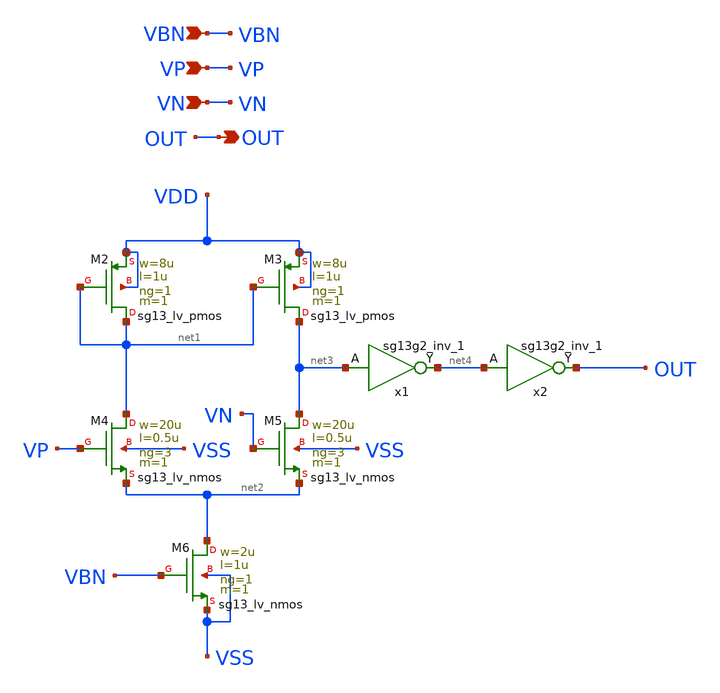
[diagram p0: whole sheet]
** sch_path: design/blocks/comparator/schematic/comp_sup.sch
**.subckt comp_sup OUT VN VP VBN
*.opin OUT
*.ipin VN
*.ipin VP
*.ipin VBN
XM2 net1 net1 VDD VDD sg13_lv_pmos w=8u l=1u ng=1 m=1 mm_ok=1
XM3 net3 net1 VDD VDD sg13_lv_pmos w=8u l=1u ng=1 m=1 mm_ok=1
XM4 net1 VP net2 VSS sg13_lv_nmos w=20u l=0.5u ng=3 m=1 mm_ok=1
XM5 net3 VN net2 VSS sg13_lv_nmos w=20u l=0.5u ng=3 m=1 mm_ok=1
XM6 net2 VBN VSS VSS sg13_lv_nmos w=2u l=1u ng=1 m=1 mm_ok=1
x1 net4 net3 VDD VSS sg13g2_inv_1
x2 OUT net4 VDD VSS sg13g2_inv_1
**.ends

* expanding   symbol:  sg13g2_inv_1.sym # of pins=2
** sym_path: sg13g2_inv_1.sym
** sch_path: sg13g2_inv_1.sch
.subckt sg13g2_inv_1 Y A VDD VSS
*.opin Y
*.ipin A
*.iopin VDD
*.iopin VSS
XM1 Y A VSS VSS sg13_lv_nmos w=740.00n l=130.00n ng=1 m=1 mm_ok=1
XM2 Y A VDD VDD sg13_lv_pmos w=1.12u l=130.00n ng=1 m=1 mm_ok=1
.ends

.end
